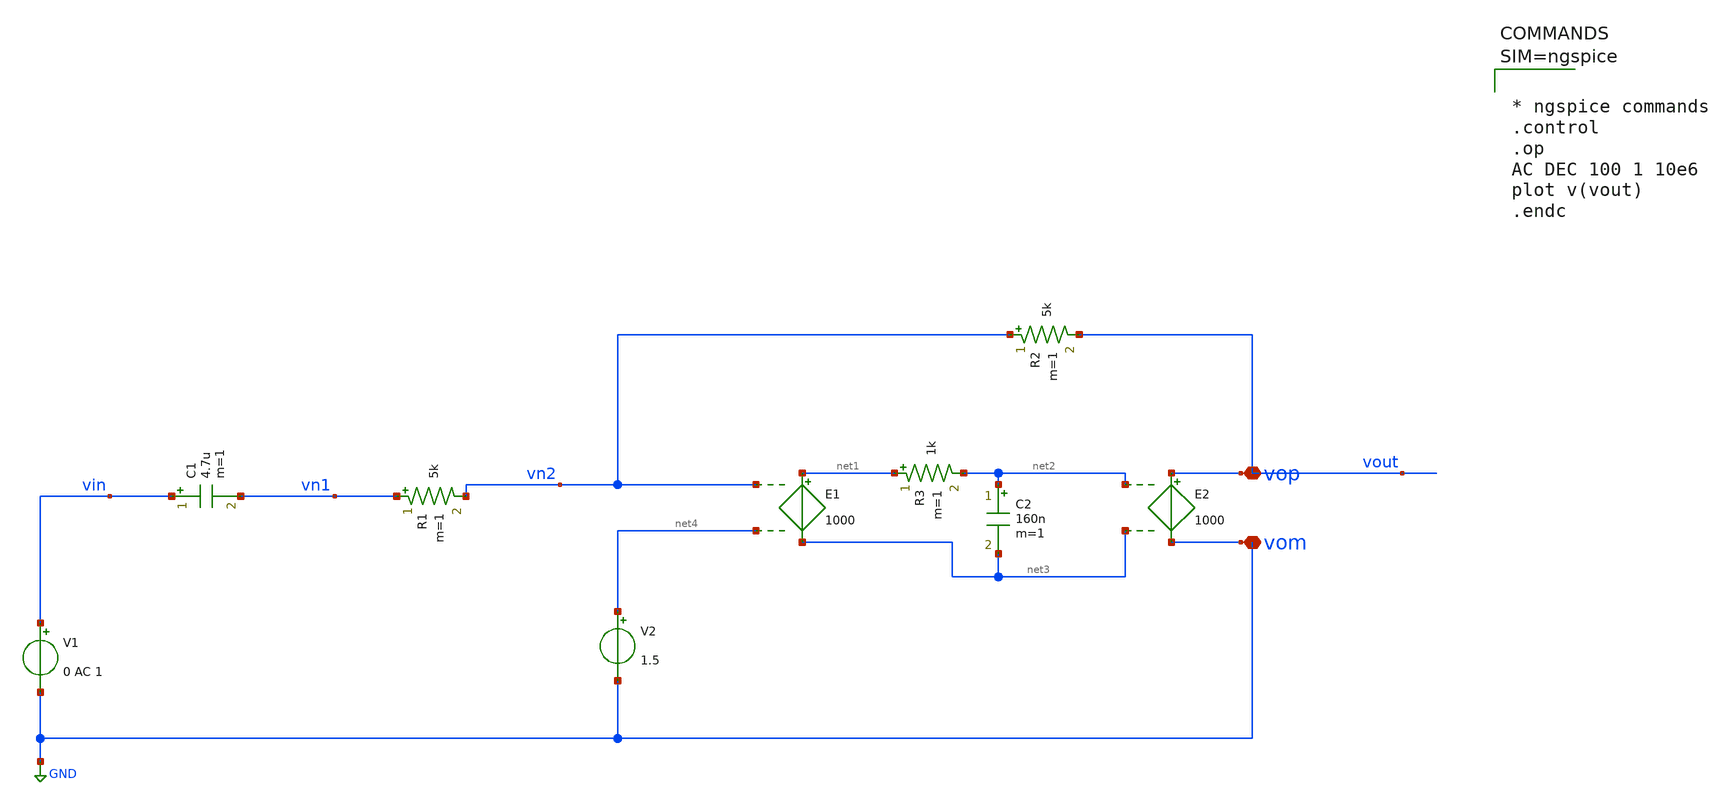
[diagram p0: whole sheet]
** sch_path: xschem/lowapss.sch
**.subckt lowapss vop vom
*.iopin vop
*.iopin vom
R1 vn1 vn2 5k m=1
R2 vn2 vout 5k m=1
C1 vin vn1 4.7u m=1
V1 vin GND 0 AC 1
V2 net4 GND 1.5
E1 net1 net3 vn2 net4 1000
E2 vop vom net2 net3 1000
R3 net1 net2 1k m=1
C2 net2 net3 160n m=1
**** begin user architecture code



* ngspice commands
.control
.op
AC DEC 100 1 10e6
plot v(vout)
.endc



**** end user architecture code
**.ends
.GLOBAL GND
.end
